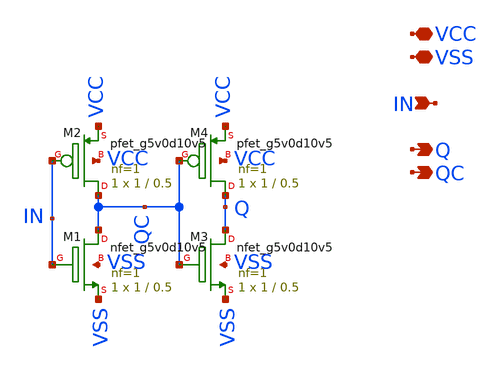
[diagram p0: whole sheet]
** sch_path: Comparator/schematic/miyahara/buf.sch
**.subckt buf VCC Q IN VSS QC
*.iopin VCC
*.opin Q
*.ipin IN
*.iopin VSS
*.opin QC
XM1 QC IN VSS VSS sky130_fd_pr__nfet_g5v0d10v5 L=0.5 W=1 nf=1 ad='int((nf+1)/2) * W/nf * 0.29' as='int((nf+2)/2) * W/nf * 0.29'
+ pd='2*int((nf+1)/2) * (W/nf + 0.29)' ps='2*int((nf+2)/2) * (W/nf + 0.29)' nrd='0.29 / W' nrs='0.29 / W'
+ sa=0 sb=0 sd=0 mult=1 m=1
XM2 QC IN VCC VCC sky130_fd_pr__pfet_g5v0d10v5 L=0.5 W=1 nf=1 ad='int((nf+1)/2) * W/nf * 0.29' as='int((nf+2)/2) * W/nf * 0.29'
+ pd='2*int((nf+1)/2) * (W/nf + 0.29)' ps='2*int((nf+2)/2) * (W/nf + 0.29)' nrd='0.29 / W' nrs='0.29 / W'
+ sa=0 sb=0 sd=0 mult=1 m=1
XM3 Q QC VSS VSS sky130_fd_pr__nfet_g5v0d10v5 L=0.5 W=1 nf=1 ad='int((nf+1)/2) * W/nf * 0.29' as='int((nf+2)/2) * W/nf * 0.29'
+ pd='2*int((nf+1)/2) * (W/nf + 0.29)' ps='2*int((nf+2)/2) * (W/nf + 0.29)' nrd='0.29 / W' nrs='0.29 / W'
+ sa=0 sb=0 sd=0 mult=1 m=1
XM4 Q QC VCC VCC sky130_fd_pr__pfet_g5v0d10v5 L=0.5 W=1 nf=1 ad='int((nf+1)/2) * W/nf * 0.29' as='int((nf+2)/2) * W/nf * 0.29'
+ pd='2*int((nf+1)/2) * (W/nf + 0.29)' ps='2*int((nf+2)/2) * (W/nf + 0.29)' nrd='0.29 / W' nrs='0.29 / W'
+ sa=0 sb=0 sd=0 mult=1 m=1
**.ends
.end
